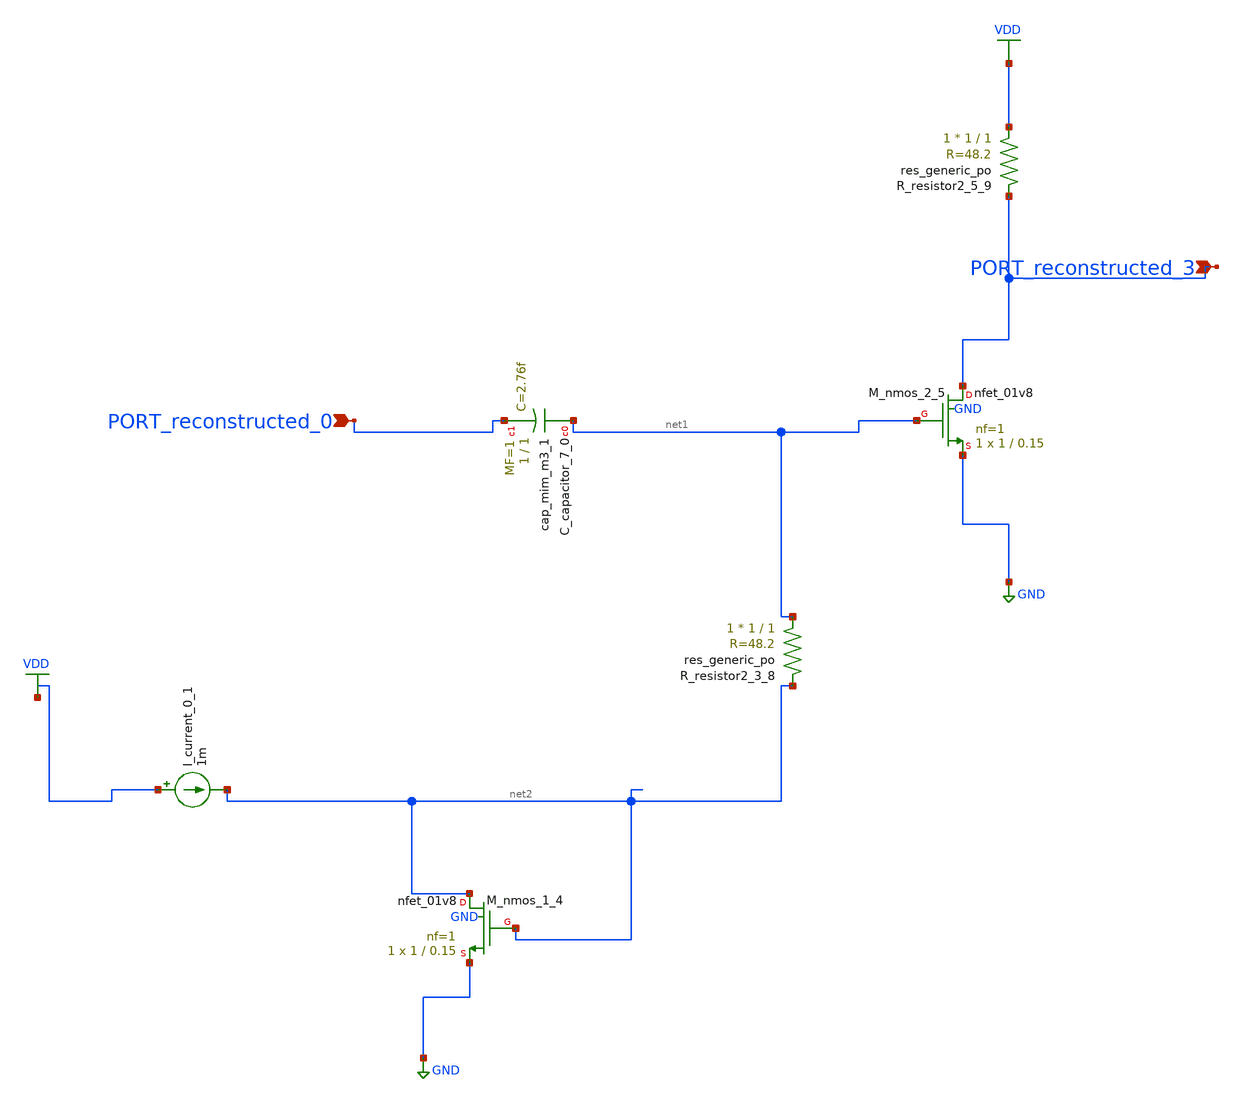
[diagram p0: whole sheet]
** sch_path: schematics/AMSNet/300.sch
**.subckt 300 PORT_reconstructed_3 PORT_reconstructed_0
*.ipin PORT_reconstructed_3
*.ipin PORT_reconstructed_0
XC_capacitor_7_0 net1 PORT_reconstructed_0 sky130_fd_pr__cap_mim_m3_1 W=1 L=1 MF=1 m=1
I_current_0_1 VDD net2 1m
XM_nmos_1_4 net2 net2 GND GND sky130_fd_pr__nfet_01v8 L=0.15 W=1 nf=1 ad='int((1 + 1)/2) * 1 / 1 * 0.29'
+ as='int((1 + 2)/2) * 1 / 1 * 0.29' pd='2*int((1 + 1)/2) * (1 / 1 + 0.29)' ps='2*int((1 + 2)/2) * (1 / 1 + 0.29)'
+ nrd='0.29 / 1 ' nrs='0.29 / 1 ' sa=0 sb=0 sd=0 mult=1 m=1
XM_nmos_2_5 PORT_reconstructed_3 net1 GND GND sky130_fd_pr__nfet_01v8 L=0.15 W=1 nf=1 ad='int((1 + 1)/2) * 1 / 1 * 0.29'
+ as='int((1 + 2)/2) * 1 / 1 * 0.29' pd='2*int((1 + 1)/2) * (1 / 1 + 0.29)' ps='2*int((1 + 2)/2) * (1 / 1 + 0.29)'
+ nrd='0.29 / 1 ' nrs='0.29 / 1 ' sa=0 sb=0 sd=0 mult=1 m=1
XR_resistor2_3_8 net1 net2 sky130_fd_pr__res_generic_po W=1 L=1 m=1
XR_resistor2_5_9 VDD PORT_reconstructed_3 sky130_fd_pr__res_generic_po W=1 L=1 m=1
**.ends
.GLOBAL GND
.GLOBAL VDD
.end
